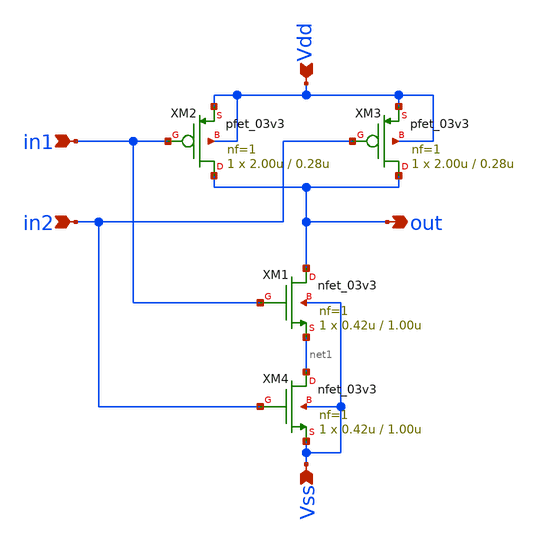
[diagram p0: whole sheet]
** sch_path: NAND/Nand_Gate/xschem/nand_gate.sch
**.subckt nand_gate in1 out Vdd Vss in2
*.ipin in1
*.opin out
*.ipin Vdd
*.ipin Vss
*.ipin in2
XM3 out in2 Vdd Vdd pfet_03v3 L=0.28u W=2.00u nf=1 ad='int((nf+1)/2) * W/nf * 0.18u' as='int((nf+2)/2) * W/nf * 0.18u'
+ pd='2*int((nf+1)/2) * (W/nf + 0.18u)' ps='2*int((nf+2)/2) * (W/nf + 0.18u)' nrd='0.18u / W' nrs='0.18u / W'
+ sa=0 sb=0 sd=0 m=1
XM1 out in1 net1 Vss nfet_03v3 L=1.00u W=0.42u nf=1 ad='int((nf+1)/2) * W/nf * 0.18u' as='int((nf+2)/2) * W/nf * 0.18u'
+ pd='2*int((nf+1)/2) * (W/nf + 0.18u)' ps='2*int((nf+2)/2) * (W/nf + 0.18u)' nrd='0.18u / W' nrs='0.18u / W'
+ sa=0 sb=0 sd=0 m=1
XM2 out in1 Vdd Vdd pfet_03v3 L=0.28u W=2.00u nf=1 ad='int((nf+1)/2) * W/nf * 0.18u' as='int((nf+2)/2) * W/nf * 0.18u'
+ pd='2*int((nf+1)/2) * (W/nf + 0.18u)' ps='2*int((nf+2)/2) * (W/nf + 0.18u)' nrd='0.18u / W' nrs='0.18u / W'
+ sa=0 sb=0 sd=0 m=1
XM4 net1 in2 Vss Vss nfet_03v3 L=1.00u W=0.42u nf=1 ad='int((nf+1)/2) * W/nf * 0.18u' as='int((nf+2)/2) * W/nf * 0.18u'
+ pd='2*int((nf+1)/2) * (W/nf + 0.18u)' ps='2*int((nf+2)/2) * (W/nf + 0.18u)' nrd='0.18u / W' nrs='0.18u / W'
+ sa=0 sb=0 sd=0 m=1
**.ends
.end
